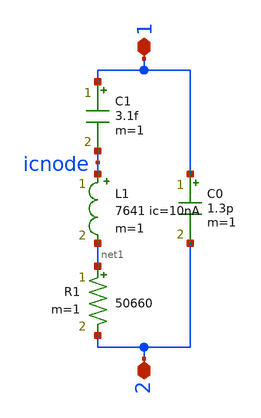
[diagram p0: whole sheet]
** sch_path: cace/xtal_iqd_125_1.sch
**.subckt xtal_iqd_125_1 1 2
*.iopin 1
*.iopin 2
L1 icnode net1 7641 ic=10nA m=1
C1 1 icnode 3.1f m=1
C0 1 2 1.3p m=1
R1 net1 2 50660 m=1
**.ends
.end
